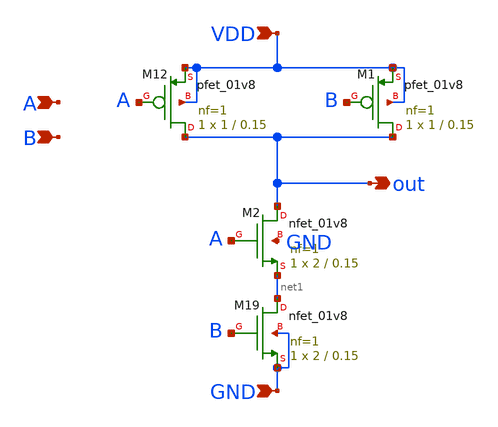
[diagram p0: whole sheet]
** sch_path: xschem/vault/NAND.sch
**.subckt NAND VDD GND out A B
*.ipin VDD
*.ipin GND
*.opin out
*.ipin A
*.ipin B
XM12 out A VDD VDD sky130_fd_pr__pfet_01v8 L=0.15 W=1 nf=1 ad='int((nf+1)/2) * W/nf * 0.29' as='int((nf+2)/2) * W/nf * 0.29'
+ pd='2*int((nf+1)/2) * (W/nf + 0.29)' ps='2*int((nf+2)/2) * (W/nf + 0.29)' nrd='0.29 / W' nrs='0.29 / W'
+ sa=0 sb=0 sd=0 mult=1 m=1
XM19 net1 B GND GND sky130_fd_pr__nfet_01v8 L=0.15 W=2 nf=1 ad='int((nf+1)/2) * W/nf * 0.29' as='int((nf+2)/2) * W/nf * 0.29'
+ pd='2*int((nf+1)/2) * (W/nf + 0.29)' ps='2*int((nf+2)/2) * (W/nf + 0.29)' nrd='0.29 / W' nrs='0.29 / W'
+ sa=0 sb=0 sd=0 mult=1 m=1
XM1 out B VDD VDD sky130_fd_pr__pfet_01v8 L=0.15 W=1 nf=1 ad='int((nf+1)/2) * W/nf * 0.29' as='int((nf+2)/2) * W/nf * 0.29'
+ pd='2*int((nf+1)/2) * (W/nf + 0.29)' ps='2*int((nf+2)/2) * (W/nf + 0.29)' nrd='0.29 / W' nrs='0.29 / W'
+ sa=0 sb=0 sd=0 mult=1 m=1
XM2 out A net1 GND sky130_fd_pr__nfet_01v8 L=0.15 W=2 nf=1 ad='int((nf+1)/2) * W/nf * 0.29' as='int((nf+2)/2) * W/nf * 0.29'
+ pd='2*int((nf+1)/2) * (W/nf + 0.29)' ps='2*int((nf+2)/2) * (W/nf + 0.29)' nrd='0.29 / W' nrs='0.29 / W'
+ sa=0 sb=0 sd=0 mult=1 m=1
**.ends
.end
